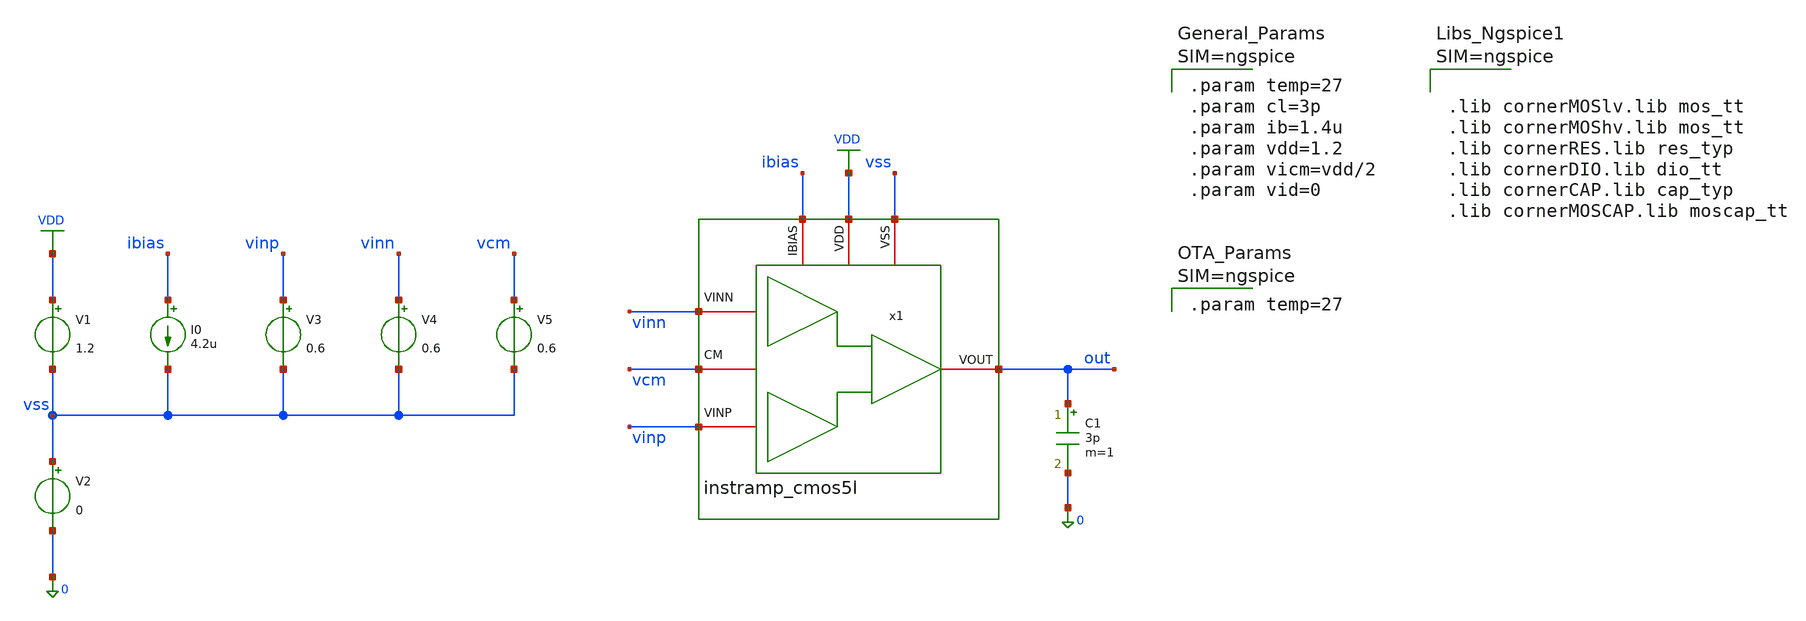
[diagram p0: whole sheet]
** sch_path: xschem/instramp_cmos5l/tb/tb_instramp_cmos5l_noise/tb_instramp_cmos5l_noise.sch
**.subckt tb_instramp_cmos5l_noise
C1 out 0 3p m=1
I0 ibias vss 4.2u
V1 VDD vss 1.2
V2 vss 0 0
V3 vinp vss 0.6
V4 vinn vss 0.6
x1 vss VDD ibias vinn out vinp vcm instramp_cmos5l
V5 vcm vss 0.6
**** begin user architecture code



.lib cornerMOSlv.lib mos_tt
.lib cornerMOShv.lib mos_tt
.lib cornerRES.lib res_typ
.lib cornerDIO.lib dio_tt
.lib cornerCAP.lib cap_typ
.lib cornerMOSCAP.lib moscap_tt





.param temp=27
.param cl=3p
.param ib=1.4u
.param vdd=1.2
.param vicm=vdd/2
.param vid=0





.param temp=27





.control
save all
destroy all
shell mkdir -p result

* Noise referred to V3 (VINP): gain VINP->OUT = Adm, so inoise = differential-input noise.
* VINN / VCM are held at DC.
alter @v3[acmag]=1
noise v(out) v3 dec 20 10 100MEG
alter @v3[acmag]=0

setplot noise1

* Parameters #1
let inoise_total_uv = noise2.inoise_total * 1e6
let onoise_total_uv = noise2.onoise_total * 1e6
let irn_nv = noise1.inoise_spectrum * 1e9
let orn_nv = noise1.onoise_spectrum * 1e9

* inoise_total integrates out to 100 MHz where the closed-loop gain has rolled off, so it is
* inflated. In-band equivalent = output noise / low-frequency gain (gain = onoise/inoise @ 10 Hz).
let gain_lf = noise1.onoise_spectrum[0] / noise1.inoise_spectrum[0]
let inoise_eq_uv = onoise_total_uv / gain_lf

* IRN extraction at certain frequencies (20 pts/dec from 10 Hz)
let irn_10 = irn_nv[0]
let irn_100 = irn_nv[20]
let irn_1k = irn_nv[40]
let irn_10k = irn_nv[60]
let irn_100k = irn_nv[80]
let irn_1meg = irn_nv[100]

write ./result/tb_instramp_cmos5l_noise.raw irn_nv orn_nv inoise_spectrum onoise_spectrum

echo "======================================================="
echo " Total Output Noise (10 Hz - 100 MHz): " $&onoise_total_uv " uV_rms"
echo " Total Input Noise (10 Hz - 100 MHz): " $&inoise_total_uv " uV_rms (inflated, see above)"
echo " In-band Input-Referred (Vout_n/Gain): " $&inoise_eq_uv " uV_rms"
echo "-------------------------------------------------------"
echo " IRN @ 10 Hz (Flicker Noise): " $&irn_10 " nV/sqrt(Hz)"
echo " IRN @ 100 Hz: " $&irn_100 " nV/sqrt(Hz)"
echo " IRN @ 1 kHz: " $&irn_1k " nV/sqrt(Hz)"
echo " IRN @ 10 kHz: " $&irn_10k " nV/sqrt(Hz)"
echo " IRN @ 100 kHz: " $&irn_100k " nV/sqrt(Hz)"
echo " IRN @ 1 MHz (Thermal Noise Floor): " $&irn_1meg " nV/sqrt(Hz)"
echo "======================================================="

plot irn_nv orn_nv loglog
.endc


**** end user architecture code
**.ends

* expanding   symbol:
*+  /foss/designs/sg13cmos5l_spma_ip__instramp/xschem/instramp_cmos5l/instramp_cmos5l.sym # of pins=7
** sym_path: /foss/designs/sg13cmos5l_spma_ip__instramp/xschem/instramp_cmos5l/instramp_cmos5l.sym
** sch_path: /foss/designs/sg13cmos5l_spma_ip__instramp/xschem/instramp_cmos5l/instramp_cmos5l.sch
.subckt instramp_cmos5l VSS VDD IBIAS VINN VOUT VINP CM
*.iopin VDD
*.iopin IBIAS
*.iopin VSS
*.iopin CM
*.iopin VOUT
*.iopin VINN
*.iopin VINP
x1 VSS IBIAS VDD net3 VINP net4 ota_cmos5l
x2 VSS IBIAS VDD net1 VINN net2 ota_cmos5l
x3 VSS IBIAS VDD net5 net6 VOUT ota_cmos5l
XR1 net4 net6 VSS rhigh w=0.5e-6 l=2e-6 m=1 b=0 mm_ok=1
XR2 net2 net5 VSS rhigh w=0.5e-6 l=2e-6 m=1 b=0 mm_ok=1
XR3 net6 CM VSS rhigh w=0.5e-6 l=8*2.23e-6 m=1 b=0 mm_ok=1
XR4 net5 VOUT VSS rhigh w=0.5e-6 l=8*2.23e-6 m=1 b=0 mm_ok=1
XR7 net2 net1 VSS rhigh w=0.5e-6 l=2e-6 m=1 b=0 mm_ok=1
XR8 net4 net3 VSS rhigh w=0.5e-6 l=2e-6 m=1 b=0 mm_ok=1
.ends


* expanding   symbol:  /foss/designs/sg13cmos5l_spma_ip__instramp/xschem/ota_cmos5l/ota_cmos5l.sym #
*+ of pins=6
** sym_path: xschem/output_buffer/ota_cmos5l.sym
** sch_path: xschem/output_buffer/ota_cmos5l.sch
.subckt ota_cmos5l VSS IBIAS VDD VINN VINP VOUT
*.iopin IBIAS
*.iopin VDD
*.iopin VSS
*.iopin VOUT
*.iopin VINP
*.iopin VINN
XM6 IBIAS IBIAS VDD VDD sg13_lv_pmos w={wbias} l={lbias} ng=1 m={m6} mm_ok=1
XM7 net1 IBIAS VDD VDD sg13_lv_pmos w={wbias} l={lbias} ng=1 m={m7} mm_ok=1
XM8 VOUT IBIAS VDD VDD sg13_lv_pmos w={wbias} l={lbias} ng=1 m={m8} mm_ok=1
XM1 net2 VINN net1 VDD sg13_lv_pmos w={winpair} l={linpair} ng=1 m=1 mm_ok=1
XM2 net3 VINP net1 VDD sg13_lv_pmos w={winpair} l={linpair} ng=1 m=1 mm_ok=1
XM3 net2 net2 VSS VSS sg13_lv_nmos w={wload} l={lload} ng=1 m=1 mm_ok=1
XM4 net3 net2 VSS VSS sg13_lv_nmos w={wload} l={lload} ng=1 m=1 mm_ok=1
XM5 VOUT net3 VSS VSS sg13_lv_nmos w={wcs} l={lcs} ng=1 m=1 mm_ok=1
XR1 net3 net4 VSS rhigh w=0.5e-6 l=1.95e-6 m=1 b=0 mm_ok=1
.save v(vinp)
.save v(vinn)
.save v(vout)
XC2 VOUT net4 cap_cmomi w=15e-6 l=15e-6 mmin=1 mmax=4 feed=double subblock=0 m=5 mm_ok=1
**** begin user architecture code


.param temp=27
.param lbias=0.15u wbias=0.15u
.param m6=1 m7=4 m8=8
.param linpair=3u winpair=20u
.param lload=5u wload=10u
.param lcs=3u wcs=20u
.param Cc=2p



**** end user architecture code
XC1 VOUT net4 cap_cmomi w=15e-6 l=15e-6 mmin=1 mmax=4 feed=double subblock=0 m=4 mm_ok=1
.ends

.GLOBAL VDD
.end
